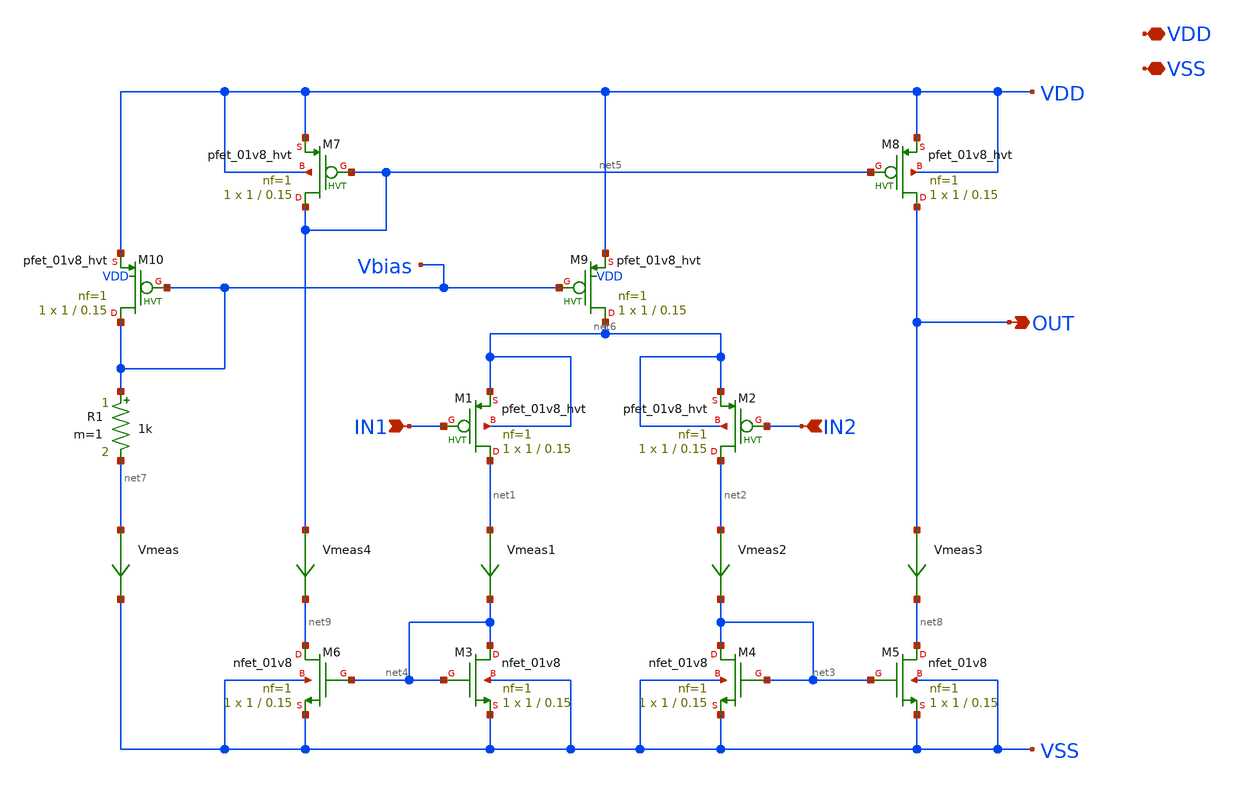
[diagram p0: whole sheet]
** sch_path: xschem/OTA_Simmetrico.sch
**.subckt OTA_Simmetrico VDD VSS IN1 IN2 OUT
*.iopin VDD
*.iopin VSS
*.ipin IN1
*.ipin IN2
*.opin OUT
XM1 net1 IN1 net6 net6 sky130_fd_pr__pfet_01v8_hvt L=0.15 W=1 nf=1 ad='int((nf+1)/2) * W/nf * 0.29' as='int((nf+2)/2) * W/nf * 0.29'
+ pd='2*int((nf+1)/2) * (W/nf + 0.29)' ps='2*int((nf+2)/2) * (W/nf + 0.29)' nrd='0.29 / W' nrs='0.29 / W'
+ sa=0 sb=0 sd=0 mult=1 m=1
XM2 net2 IN2 net6 net6 sky130_fd_pr__pfet_01v8_hvt L=0.15 W=1 nf=1 ad='int((nf+1)/2) * W/nf * 0.29' as='int((nf+2)/2) * W/nf * 0.29'
+ pd='2*int((nf+1)/2) * (W/nf + 0.29)' ps='2*int((nf+2)/2) * (W/nf + 0.29)' nrd='0.29 / W' nrs='0.29 / W'
+ sa=0 sb=0 sd=0 mult=1 m=1
XM3 net4 net4 VSS VSS sky130_fd_pr__nfet_01v8 L=0.15 W=1 nf=1 ad='int((nf+1)/2) * W/nf * 0.29' as='int((nf+2)/2) * W/nf * 0.29'
+ pd='2*int((nf+1)/2) * (W/nf + 0.29)' ps='2*int((nf+2)/2) * (W/nf + 0.29)' nrd='0.29 / W' nrs='0.29 / W'
+ sa=0 sb=0 sd=0 mult=1 m=1
XM4 net3 net3 VSS VSS sky130_fd_pr__nfet_01v8 L=0.15 W=1 nf=1 ad='int((nf+1)/2) * W/nf * 0.29' as='int((nf+2)/2) * W/nf * 0.29'
+ pd='2*int((nf+1)/2) * (W/nf + 0.29)' ps='2*int((nf+2)/2) * (W/nf + 0.29)' nrd='0.29 / W' nrs='0.29 / W'
+ sa=0 sb=0 sd=0 mult=1 m=1
XM5 net8 net3 VSS VSS sky130_fd_pr__nfet_01v8 L=0.15 W=1 nf=1 ad='int((nf+1)/2) * W/nf * 0.29' as='int((nf+2)/2) * W/nf * 0.29'
+ pd='2*int((nf+1)/2) * (W/nf + 0.29)' ps='2*int((nf+2)/2) * (W/nf + 0.29)' nrd='0.29 / W' nrs='0.29 / W'
+ sa=0 sb=0 sd=0 mult=1 m=1
XM6 net9 net4 VSS VSS sky130_fd_pr__nfet_01v8 L=0.15 W=1 nf=1 ad='int((nf+1)/2) * W/nf * 0.29' as='int((nf+2)/2) * W/nf * 0.29'
+ pd='2*int((nf+1)/2) * (W/nf + 0.29)' ps='2*int((nf+2)/2) * (W/nf + 0.29)' nrd='0.29 / W' nrs='0.29 / W'
+ sa=0 sb=0 sd=0 mult=1 m=1
XM7 net5 net5 VDD VDD sky130_fd_pr__pfet_01v8_hvt L=0.15 W=1 nf=1 ad='int((nf+1)/2) * W/nf * 0.29' as='int((nf+2)/2) * W/nf * 0.29'
+ pd='2*int((nf+1)/2) * (W/nf + 0.29)' ps='2*int((nf+2)/2) * (W/nf + 0.29)' nrd='0.29 / W' nrs='0.29 / W'
+ sa=0 sb=0 sd=0 mult=1 m=1
XM8 OUT net5 VDD VDD sky130_fd_pr__pfet_01v8_hvt L=0.15 W=1 nf=1 ad='int((nf+1)/2) * W/nf * 0.29' as='int((nf+2)/2) * W/nf * 0.29'
+ pd='2*int((nf+1)/2) * (W/nf + 0.29)' ps='2*int((nf+2)/2) * (W/nf + 0.29)' nrd='0.29 / W' nrs='0.29 / W'
+ sa=0 sb=0 sd=0 mult=1 m=1
XM9 net6 Vbias VDD VDD sky130_fd_pr__pfet_01v8_hvt L=0.15 W=1 nf=1 ad='int((nf+1)/2) * W/nf * 0.29' as='int((nf+2)/2) * W/nf * 0.29'
+ pd='2*int((nf+1)/2) * (W/nf + 0.29)' ps='2*int((nf+2)/2) * (W/nf + 0.29)' nrd='0.29 / W' nrs='0.29 / W'
+ sa=0 sb=0 sd=0 mult=1 m=1
XM10 Vbias Vbias VDD VDD sky130_fd_pr__pfet_01v8_hvt L=0.15 W=1 nf=1 ad='int((nf+1)/2) * W/nf * 0.29'
+ as='int((nf+2)/2) * W/nf * 0.29' pd='2*int((nf+1)/2) * (W/nf + 0.29)' ps='2*int((nf+2)/2) * (W/nf + 0.29)'
+ nrd='0.29 / W' nrs='0.29 / W' sa=0 sb=0 sd=0 mult=1 m=1
R1 Vbias net7 1k m=1
Vmeas net7 VSS 0
.save i(vmeas)
Vmeas1 net1 net4 0
.save i(vmeas1)
Vmeas2 net2 net3 0
.save i(vmeas2)
Vmeas3 OUT net8 0
.save i(vmeas3)
Vmeas4 net5 net9 0
.save i(vmeas4)
**.ends
.end
